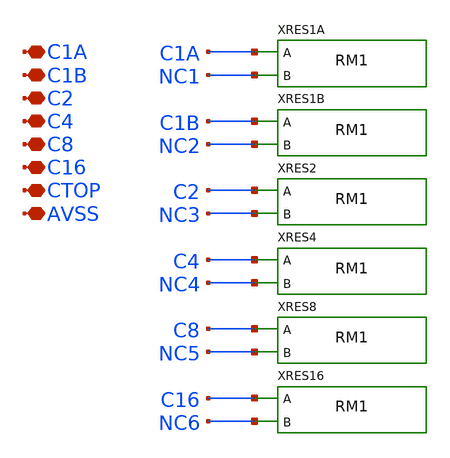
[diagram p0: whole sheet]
** sch_path: ip/sun_sar9b_sky130nm/design/SUN_SAR9B_SK130NM/CAP32C_CV.sch
**.subckt CAP32C_CV C1A C1B C2 C4 C8 C16 CTOP AVSS
*.iopin C1A
*.iopin C1B
*.iopin C2
*.iopin C4
*.iopin C8
*.iopin C16
*.iopin CTOP
*.iopin AVSS
XRES1A C1A NC1 RM1
XRES1B C1B NC2 RM1
XRES2 C2 NC3 RM1
XRES4 C4 NC4 RM1
XRES8 C8 NC5 RM1
XRES16 C16 NC6 RM1
**.ends
.end
